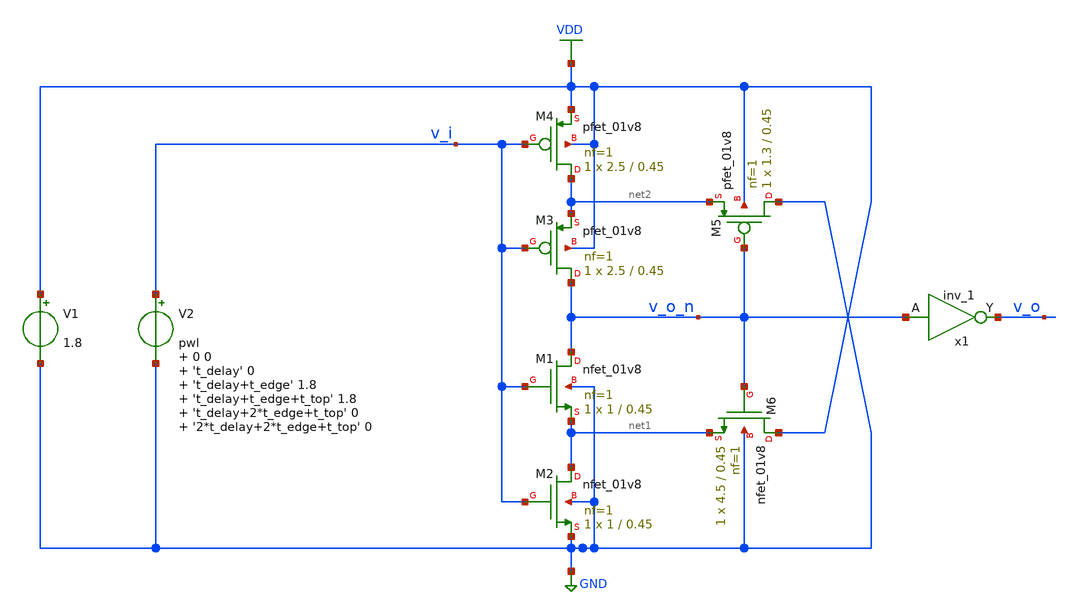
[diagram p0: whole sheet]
** sch_path: ngspice-meas-table-mc.sch
.lib $::SKYWATER_MODELS/sky130.lib.spice mc
.include $::SKYWATER_STDCELLS/sky130_fd_sc_hd.spice
**.subckt ngspice-meas-table-mc
V1 VDD GND 1.8
V2 v_i GND pwl 0 0 't_delay' 0 't_delay+t_edge' 1.8 't_delay+t_edge+t_top' 1.8 't_delay+2*t_edge+t_top'
+ 0 '2*t_delay+2*t_edge+t_top' 0
x1 v_o_n GND GND VDD VDD v_o sky130_fd_sc_hd__inv_1
XM4 net2 v_i VDD VDD sky130_fd_pr__pfet_01v8 L=0.45 W=2.5 nf=1 ad='int((nf+1)/2) * W/nf * 0.29' as='int((nf+2)/2) * W/nf * 0.29'
+ pd='2*int((nf+1)/2) * (W/nf + 0.29)' ps='2*int((nf+2)/2) * (W/nf + 0.29)' nrd='0.29 / W' nrs='0.29 / W'
+ sa=0 sb=0 sd=0 mult=1 m=1
XM5 GND v_o_n net2 VDD sky130_fd_pr__pfet_01v8 L=0.45 W=1.3 nf=1 ad='int((nf+1)/2) * W/nf * 0.29' as='int((nf+2)/2) * W/nf * 0.29'
+ pd='2*int((nf+1)/2) * (W/nf + 0.29)' ps='2*int((nf+2)/2) * (W/nf + 0.29)' nrd='0.29 / W' nrs='0.29 / W'
+ sa=0 sb=0 sd=0 mult=1 m=1
XM6 VDD v_o_n net1 GND sky130_fd_pr__nfet_01v8 L=0.45 W=4.5 nf=1 ad='int((nf+1)/2) * W/nf * 0.29' as='int((nf+2)/2) * W/nf * 0.29'
+ pd='2*int((nf+1)/2) * (W/nf + 0.29)' ps='2*int((nf+2)/2) * (W/nf + 0.29)' nrd='0.29 / W' nrs='0.29 / W'
+ sa=0 sb=0 sd=0 mult=1 m=1
XM1 v_o_n v_i net1 GND sky130_fd_pr__nfet_01v8 L=0.45 W=1 nf=1 ad='int((nf+1)/2) * W/nf * 0.29' as='int((nf+2)/2) * W/nf * 0.29'
+ pd='2*int((nf+1)/2) * (W/nf + 0.29)' ps='2*int((nf+2)/2) * (W/nf + 0.29)' nrd='0.29 / W' nrs='0.29 / W'
+ sa=0 sb=0 sd=0 mult=1 m=1
XM2 net1 v_i GND GND sky130_fd_pr__nfet_01v8 L=0.45 W=1 nf=1 ad='int((nf+1)/2) * W/nf * 0.29' as='int((nf+2)/2) * W/nf * 0.29'
+ pd='2*int((nf+1)/2) * (W/nf + 0.29)' ps='2*int((nf+2)/2) * (W/nf + 0.29)' nrd='0.29 / W' nrs='0.29 / W'
+ sa=0 sb=0 sd=0 mult=1 m=1
XM3 v_o_n v_i net2 VDD sky130_fd_pr__pfet_01v8 L=0.45 W=2.5 nf=1 ad='int((nf+1)/2) * W/nf * 0.29' as='int((nf+2)/2) * W/nf * 0.29'
+ pd='2*int((nf+1)/2) * (W/nf + 0.29)' ps='2*int((nf+2)/2) * (W/nf + 0.29)' nrd='0.29 / W' nrs='0.29 / W'
+ sa=0 sb=0 sd=0 mult=1 m=1
**** begin user architecture code


.param t_delay=1n
.param t_edge=10p
.param t_top=1n
.control
	save all
	setseed 100
	reset

	let mc_points=10
	let index=0

	setplot new
	set myplot=$curplot
	let index_mc=vector(mc_points)
	let t_pd_l2h=vector(mc_points)
	let t_pd_h2l=vector(mc_points)

	while index < mc_points
		tran 0.1p 3n

		MEAS TRAN t_pd_L2H TRIG V(v_i) VAL=0.9 RISE=1 TARG V(v_o) VAL=0.9 RISE=1
		MEAS TRAN t_pd_H2L TRIG V(v_i) VAL=0.9 FALL=1 TARG V(v_o) VAL=0.9 FALL=1

		let {$myplot}.index_mc[index]=index
		let {$myplot}.t_pd_l2h[index]=t_pd_l2h
		let {$myplot}.t_pd_h2l[index]=t_pd_h2l

		write ngspice-meas-table-mc.raw
		set appendwrite

		let index = index + 1
		reset
	end
	unset appendwrite

	setplot $myplot
	settype notype index_mc
	settype time t_pd_l2h
	settype time t_pd_h2l
	setscale index_mc
	write ngspice-meas-table-mc-meas.raw
.endc


**** end user architecture code
**.ends
.GLOBAL GND
.GLOBAL VDD
.end
